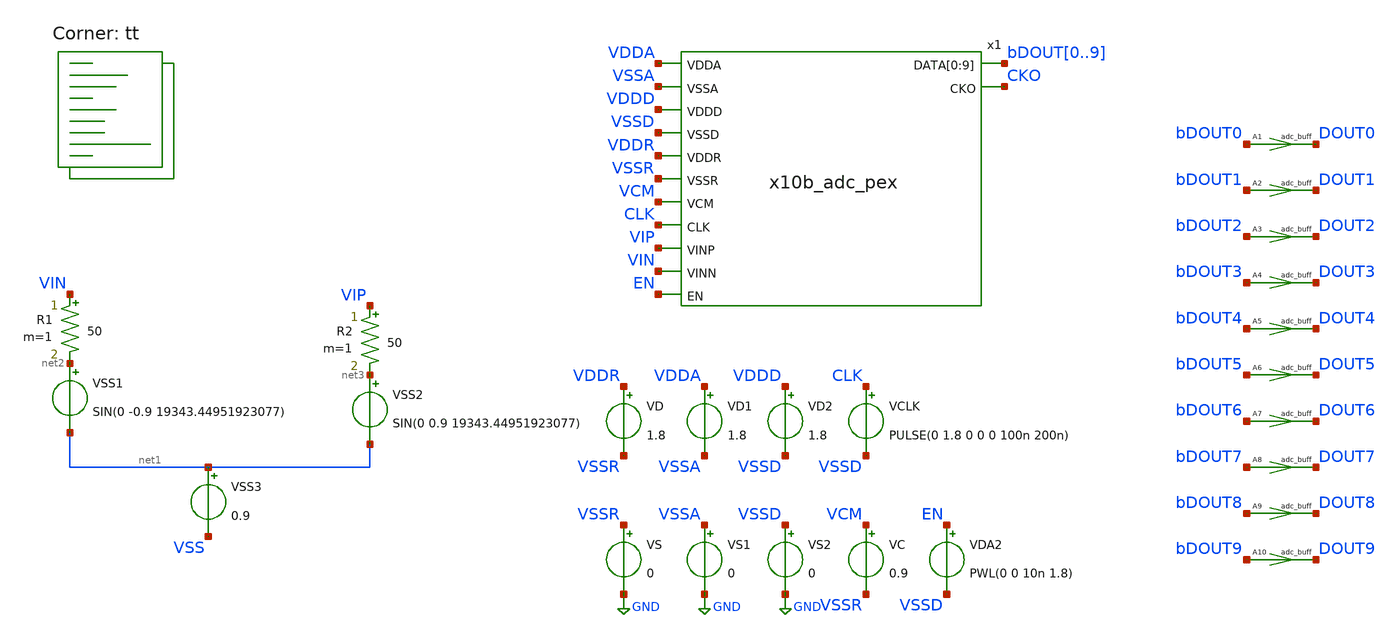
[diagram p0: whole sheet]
** sch_path: xschem/adc_tb.pex.sch
**.subckt adc_tb.pex
VS VSSR GND 0
VD VDDR VSSR 1.8
VSS1 net2 net1 SIN(0 -0.9 19343.44951923077)
VSS2 net3 net1 SIN(0 0.9 19343.44951923077)
VSS3 net1 VSS 0.9
VCLK CLK VSSD PULSE(0 1.8 0 0 0 100n 200n)
R1 VIN net2 50 m=1
R2 VIP net3 50 m=1
x1 VDDA VSSA VDDD VSSD VDDR VSSR VCM CLK VIP VIN EN bDOUT0 bDOUT1 bDOUT2 bDOUT3 bDOUT4 bDOUT5 bDOUT6
+ bDOUT7 bDOUT8 bDOUT9 CKO x10b_adc_pex
VC VCM VSSR 0.9
VDA2 EN VSSD PWL(0 0 10n 1.8)
A1 [ bDOUT0 ] [ DOUT0 ] adc_buff
A2 [ bDOUT1 ] [ DOUT1 ] adc_buff
A3 [ bDOUT2 ] [ DOUT2 ] adc_buff
A4 [ bDOUT3 ] [ DOUT3 ] adc_buff
A5 [ bDOUT4 ] [ DOUT4 ] adc_buff
A6 [ bDOUT5 ] [ DOUT5 ] adc_buff
A7 [ bDOUT6 ] [ DOUT6 ] adc_buff
A8 [ bDOUT7 ] [ DOUT7 ] adc_buff
A9 [ bDOUT8 ] [ DOUT8 ] adc_buff
A10 [ bDOUT9 ] [ DOUT9 ] adc_buff
VS1 VSSA GND 0
VD1 VDDA VSSA 1.8
VS2 VSSD GND 0
VD2 VDDD VSSD 1.8
**** begin user architecture code

** opencircuitdesign pdks install
* .lib $::SKYWATER_MODELS/sky130.lib.spice tt
*.include $PDK_ROOT/$PDK/libs.ref/sky130_fd_sc_hdll/spice/sky130_fd_sc_hdll.spice
.include $PDK_ROOT/$PDK/libs.ref/sky130_fd_sc_hs/spice/sky130_fd_sc_hs.spice
*.include $PDK_ROOT/$PDK/libs.ref/sky130_fd_sc_hd/spice/sky130_fd_sc_hd.spice



.option wnflag=0 bypass=1
.options method=trap rawfile=binary
.options solver=klu nomod
Eout out 0 VALUE = { ((V(dout0)*512 + V(dout1)*256 + V(dout2)*128 + V(dout3)*64 + V(dout4)*32 + V(dout5)*16 + V(dout6)*8 + V(dout7)*4 + V(dout8)*2 + V(dout9)*1)/3.3) - 512 }
Epowa pow_a 0 VALUE = { V(vdda)*(-i(vd1)) }
Epowd pow_d 0 VALUE = { V(vddd)*(-i(vd2)) }
Epowr pow_r 0 VALUE = { V(vddr)*(-i(vd)) }
.model adc_buff adc_bridge(in_low=0.18 in_high=1.62 rise_delay=100p fall_delay=100p)
.control
global netlist_dir .
set num_threads=16
save cko out pow_a pow_d pow_r vip vin x1.th_dif_sw_0.VCP x1.th_dif_sw_0.VCN  x1.sar10b_0.CF[0]
+  x1.sar10b_0.CF[1]  x1.sar10b_0.CF[2]  x1.sar10b_0.CF[3]  x1.sar10b_0.CF[4]  x1.sar10b_0.CF[5]  x1.sar10b_0.CF[6]
+  x1.sar10b_0.CF[7]  x1.sar10b_0.CF[8]  x1.sar10b_0.CF[9]  x1.tdc_0.RDY
tran 1n 5350u 0 uic; Mengubah start time menjadi 10n
rusage traniter trantime
meas tran avg_pow  AVG pow_a from=1n to=535u
meas tran avg_pow  AVG pow_d from=1n to=535u
meas tran avg_pow  AVG pow_r from=1n to=535u
remzerovec
write adc10b_tb_dynamic_pex.raw
wrdata adc10b_tb_dynamic_pex.txt out cko pow_a pow_d pow_r vip vin
quit 1
.endc


.lib $::SKYWATER_MODELS/sky130.lib.spice tt
**** end user architecture code
**.ends

* expanding   symbol:  x10b_adc_pex.sym # of pins=13
** sym_path: xschem/x10b_adc_pex.sym
.include /home/mthudaa/vlsi/8bit_SAR-ADC_ITS/xschem/x10b_adc_pex.spice
.GLOBAL GND
.end
